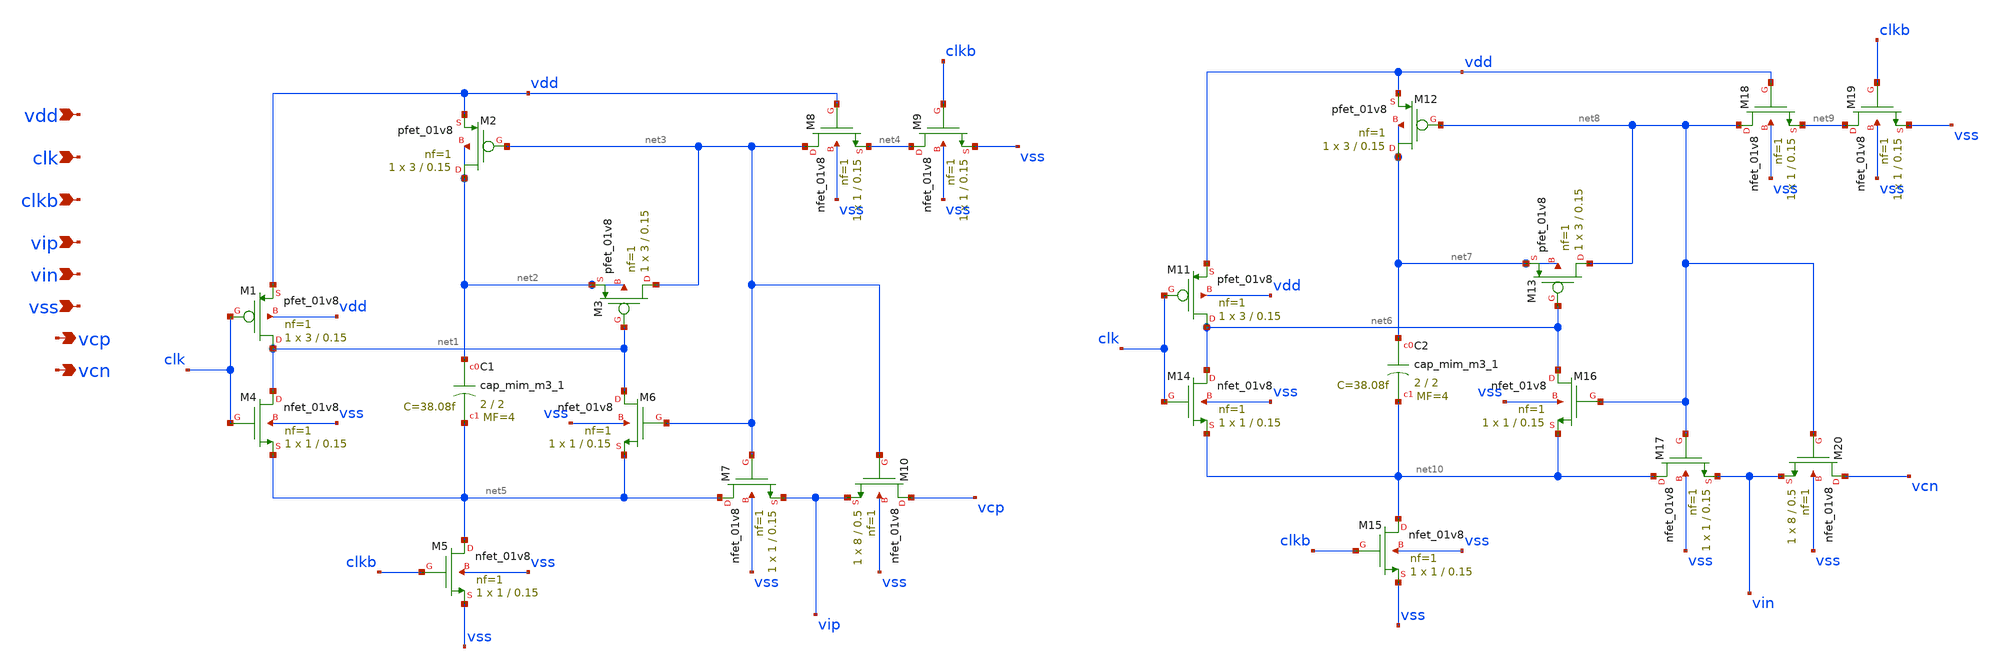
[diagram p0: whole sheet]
** sch_path: xschem/bsw_diff.sch
**.subckt bsw_diff vdd clk clkb vip vin vss vcp vcn
*.ipin vdd
*.ipin clk
*.ipin clkb
*.ipin vip
*.ipin vin
*.ipin vss
*.opin vcp
*.opin vcn
XM1 net1 clk vdd vdd sky130_fd_pr__pfet_01v8 L=0.15 W=3 nf=1 ad='int((nf+1)/2) * W/nf * 0.29' as='int((nf+2)/2) * W/nf * 0.29'
+ pd='2*int((nf+1)/2) * (W/nf + 0.29)' ps='2*int((nf+2)/2) * (W/nf + 0.29)' nrd='0.29 / W' nrs='0.29 / W'
+ sa=0 sb=0 sd=0 mult=1 m=1
XM2 net2 net3 vdd net2 sky130_fd_pr__pfet_01v8 L=0.15 W=3 nf=1 ad='int((nf+1)/2) * W/nf * 0.29' as='int((nf+2)/2) * W/nf * 0.29'
+ pd='2*int((nf+1)/2) * (W/nf + 0.29)' ps='2*int((nf+2)/2) * (W/nf + 0.29)' nrd='0.29 / W' nrs='0.29 / W'
+ sa=0 sb=0 sd=0 mult=1 m=1
XM3 net3 net1 net2 net2 sky130_fd_pr__pfet_01v8 L=0.15 W=3 nf=1 ad='int((nf+1)/2) * W/nf * 0.29' as='int((nf+2)/2) * W/nf * 0.29'
+ pd='2*int((nf+1)/2) * (W/nf + 0.29)' ps='2*int((nf+2)/2) * (W/nf + 0.29)' nrd='0.29 / W' nrs='0.29 / W'
+ sa=0 sb=0 sd=0 mult=1 m=1
XM4 net1 clk net5 vss sky130_fd_pr__nfet_01v8 L=0.15 W=1 nf=1 ad='int((nf+1)/2) * W/nf * 0.29' as='int((nf+2)/2) * W/nf * 0.29'
+ pd='2*int((nf+1)/2) * (W/nf + 0.29)' ps='2*int((nf+2)/2) * (W/nf + 0.29)' nrd='0.29 / W' nrs='0.29 / W'
+ sa=0 sb=0 sd=0 mult=1 m=1
XM5 net5 clkb vss vss sky130_fd_pr__nfet_01v8 L=0.15 W=1 nf=1 ad='int((nf+1)/2) * W/nf * 0.29' as='int((nf+2)/2) * W/nf * 0.29'
+ pd='2*int((nf+1)/2) * (W/nf + 0.29)' ps='2*int((nf+2)/2) * (W/nf + 0.29)' nrd='0.29 / W' nrs='0.29 / W'
+ sa=0 sb=0 sd=0 mult=1 m=1
XM6 net1 net3 net5 vss sky130_fd_pr__nfet_01v8 L=0.15 W=1 nf=1 ad='int((nf+1)/2) * W/nf * 0.29' as='int((nf+2)/2) * W/nf * 0.29'
+ pd='2*int((nf+1)/2) * (W/nf + 0.29)' ps='2*int((nf+2)/2) * (W/nf + 0.29)' nrd='0.29 / W' nrs='0.29 / W'
+ sa=0 sb=0 sd=0 mult=1 m=1
XM7 net5 net3 vip vss sky130_fd_pr__nfet_01v8 L=0.15 W=1 nf=1 ad='int((nf+1)/2) * W/nf * 0.29' as='int((nf+2)/2) * W/nf * 0.29'
+ pd='2*int((nf+1)/2) * (W/nf + 0.29)' ps='2*int((nf+2)/2) * (W/nf + 0.29)' nrd='0.29 / W' nrs='0.29 / W'
+ sa=0 sb=0 sd=0 mult=1 m=1
XM8 net3 vdd net4 vss sky130_fd_pr__nfet_01v8 L=0.15 W=1 nf=1 ad='int((nf+1)/2) * W/nf * 0.29' as='int((nf+2)/2) * W/nf * 0.29'
+ pd='2*int((nf+1)/2) * (W/nf + 0.29)' ps='2*int((nf+2)/2) * (W/nf + 0.29)' nrd='0.29 / W' nrs='0.29 / W'
+ sa=0 sb=0 sd=0 mult=1 m=1
XM9 net4 clkb vss vss sky130_fd_pr__nfet_01v8 L=0.15 W=1 nf=1 ad='int((nf+1)/2) * W/nf * 0.29' as='int((nf+2)/2) * W/nf * 0.29'
+ pd='2*int((nf+1)/2) * (W/nf + 0.29)' ps='2*int((nf+2)/2) * (W/nf + 0.29)' nrd='0.29 / W' nrs='0.29 / W'
+ sa=0 sb=0 sd=0 mult=1 m=1
XC1 net2 net5 sky130_fd_pr__cap_mim_m3_1 W=2 L=2 MF=4 m=4
XM10 vcp net3 vip vss sky130_fd_pr__nfet_01v8 L=0.5 W=8 nf=1 ad='int((nf+1)/2) * W/nf * 0.29' as='int((nf+2)/2) * W/nf * 0.29'
+ pd='2*int((nf+1)/2) * (W/nf + 0.29)' ps='2*int((nf+2)/2) * (W/nf + 0.29)' nrd='0.29 / W' nrs='0.29 / W'
+ sa=0 sb=0 sd=0 mult=1 m=1
XM11 net6 clk vdd vdd sky130_fd_pr__pfet_01v8 L=0.15 W=3 nf=1 ad='int((nf+1)/2) * W/nf * 0.29' as='int((nf+2)/2) * W/nf * 0.29'
+ pd='2*int((nf+1)/2) * (W/nf + 0.29)' ps='2*int((nf+2)/2) * (W/nf + 0.29)' nrd='0.29 / W' nrs='0.29 / W'
+ sa=0 sb=0 sd=0 mult=1 m=1
XM12 net7 net8 vdd net7 sky130_fd_pr__pfet_01v8 L=0.15 W=3 nf=1 ad='int((nf+1)/2) * W/nf * 0.29' as='int((nf+2)/2) * W/nf * 0.29'
+ pd='2*int((nf+1)/2) * (W/nf + 0.29)' ps='2*int((nf+2)/2) * (W/nf + 0.29)' nrd='0.29 / W' nrs='0.29 / W'
+ sa=0 sb=0 sd=0 mult=1 m=1
XM13 net8 net6 net7 net7 sky130_fd_pr__pfet_01v8 L=0.15 W=3 nf=1 ad='int((nf+1)/2) * W/nf * 0.29' as='int((nf+2)/2) * W/nf * 0.29'
+ pd='2*int((nf+1)/2) * (W/nf + 0.29)' ps='2*int((nf+2)/2) * (W/nf + 0.29)' nrd='0.29 / W' nrs='0.29 / W'
+ sa=0 sb=0 sd=0 mult=1 m=1
XM14 net6 clk net10 vss sky130_fd_pr__nfet_01v8 L=0.15 W=1 nf=1 ad='int((nf+1)/2) * W/nf * 0.29' as='int((nf+2)/2) * W/nf * 0.29'
+ pd='2*int((nf+1)/2) * (W/nf + 0.29)' ps='2*int((nf+2)/2) * (W/nf + 0.29)' nrd='0.29 / W' nrs='0.29 / W'
+ sa=0 sb=0 sd=0 mult=1 m=1
XM15 net10 clkb vss vss sky130_fd_pr__nfet_01v8 L=0.15 W=1 nf=1 ad='int((nf+1)/2) * W/nf * 0.29' as='int((nf+2)/2) * W/nf * 0.29'
+ pd='2*int((nf+1)/2) * (W/nf + 0.29)' ps='2*int((nf+2)/2) * (W/nf + 0.29)' nrd='0.29 / W' nrs='0.29 / W'
+ sa=0 sb=0 sd=0 mult=1 m=1
XM16 net6 net8 net10 vss sky130_fd_pr__nfet_01v8 L=0.15 W=1 nf=1 ad='int((nf+1)/2) * W/nf * 0.29' as='int((nf+2)/2) * W/nf * 0.29'
+ pd='2*int((nf+1)/2) * (W/nf + 0.29)' ps='2*int((nf+2)/2) * (W/nf + 0.29)' nrd='0.29 / W' nrs='0.29 / W'
+ sa=0 sb=0 sd=0 mult=1 m=1
XM17 net10 net8 vin vss sky130_fd_pr__nfet_01v8 L=0.15 W=1 nf=1 ad='int((nf+1)/2) * W/nf * 0.29' as='int((nf+2)/2) * W/nf * 0.29'
+ pd='2*int((nf+1)/2) * (W/nf + 0.29)' ps='2*int((nf+2)/2) * (W/nf + 0.29)' nrd='0.29 / W' nrs='0.29 / W'
+ sa=0 sb=0 sd=0 mult=1 m=1
XM18 net8 vdd net9 vss sky130_fd_pr__nfet_01v8 L=0.15 W=1 nf=1 ad='int((nf+1)/2) * W/nf * 0.29' as='int((nf+2)/2) * W/nf * 0.29'
+ pd='2*int((nf+1)/2) * (W/nf + 0.29)' ps='2*int((nf+2)/2) * (W/nf + 0.29)' nrd='0.29 / W' nrs='0.29 / W'
+ sa=0 sb=0 sd=0 mult=1 m=1
XM19 net9 clkb vss vss sky130_fd_pr__nfet_01v8 L=0.15 W=1 nf=1 ad='int((nf+1)/2) * W/nf * 0.29' as='int((nf+2)/2) * W/nf * 0.29'
+ pd='2*int((nf+1)/2) * (W/nf + 0.29)' ps='2*int((nf+2)/2) * (W/nf + 0.29)' nrd='0.29 / W' nrs='0.29 / W'
+ sa=0 sb=0 sd=0 mult=1 m=1
XC2 net7 net10 sky130_fd_pr__cap_mim_m3_1 W=2 L=2 MF=4 m=4
XM20 vcn net8 vin vss sky130_fd_pr__nfet_01v8 L=0.5 W=8 nf=1 ad='int((nf+1)/2) * W/nf * 0.29' as='int((nf+2)/2) * W/nf * 0.29'
+ pd='2*int((nf+1)/2) * (W/nf + 0.29)' ps='2*int((nf+2)/2) * (W/nf + 0.29)' nrd='0.29 / W' nrs='0.29 / W'
+ sa=0 sb=0 sd=0 mult=1 m=1
**.ends
.end
